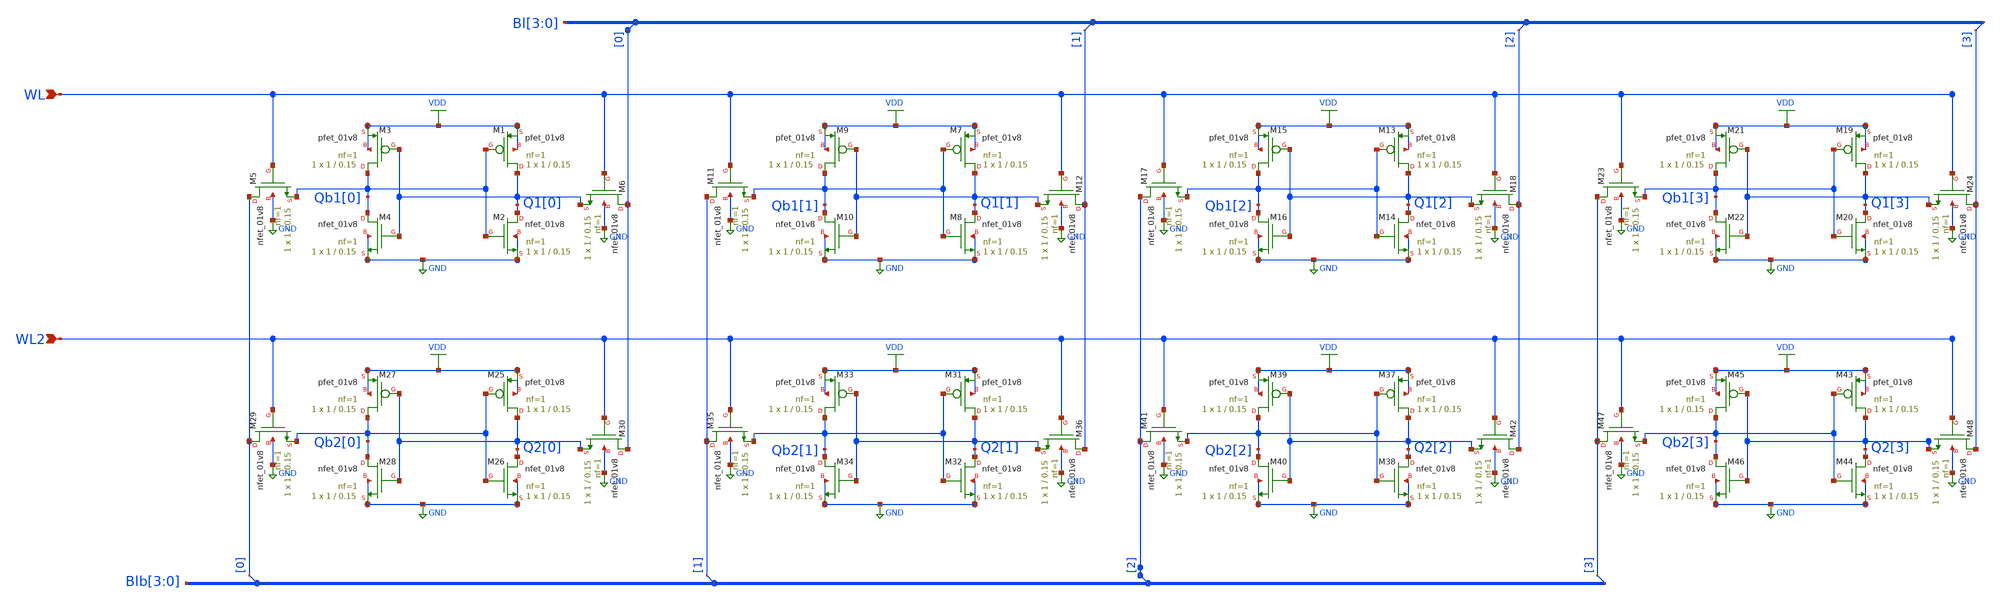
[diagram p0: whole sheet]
** sch_path: Circuit Files/circuits/circuits/RAM8BIT.sch
**.subckt RAM8BIT WL WL2
*.ipin WL
*.ipin WL2
XM1 Q1[0] Qb1[0] VDD VDD sky130_fd_pr__pfet_01v8 L=0.15 W=1 nf=1 ad='int((nf+1)/2) * W/nf * 0.29' as='int((nf+2)/2) * W/nf * 0.29'
+ pd='2*int((nf+1)/2) * (W/nf + 0.29)' ps='2*int((nf+2)/2) * (W/nf + 0.29)' nrd='0.29 / W' nrs='0.29 / W'
+ sa=0 sb=0 sd=0 mult=1 m=1
XM2 Q1[0] Qb1[0] GND GND sky130_fd_pr__nfet_01v8 L=0.15 W=1 nf=1 ad='int((nf+1)/2) * W/nf * 0.29' as='int((nf+2)/2) * W/nf * 0.29'
+ pd='2*int((nf+1)/2) * (W/nf + 0.29)' ps='2*int((nf+2)/2) * (W/nf + 0.29)' nrd='0.29 / W' nrs='0.29 / W'
+ sa=0 sb=0 sd=0 mult=1 m=1
XM3 Qb1[0] Q1[0] VDD VDD sky130_fd_pr__pfet_01v8 L=0.15 W=1 nf=1 ad='int((nf+1)/2) * W/nf * 0.29' as='int((nf+2)/2) * W/nf * 0.29'
+ pd='2*int((nf+1)/2) * (W/nf + 0.29)' ps='2*int((nf+2)/2) * (W/nf + 0.29)' nrd='0.29 / W' nrs='0.29 / W'
+ sa=0 sb=0 sd=0 mult=1 m=1
XM4 Qb1[0] Q1[0] GND GND sky130_fd_pr__nfet_01v8 L=0.15 W=1 nf=1 ad='int((nf+1)/2) * W/nf * 0.29' as='int((nf+2)/2) * W/nf * 0.29'
+ pd='2*int((nf+1)/2) * (W/nf + 0.29)' ps='2*int((nf+2)/2) * (W/nf + 0.29)' nrd='0.29 / W' nrs='0.29 / W'
+ sa=0 sb=0 sd=0 mult=1 m=1
XM5 Blb[0] WL Qb1[0] GND sky130_fd_pr__nfet_01v8 L=0.15 W=1 nf=1 ad='int((nf+1)/2) * W/nf * 0.29' as='int((nf+2)/2) * W/nf * 0.29'
+ pd='2*int((nf+1)/2) * (W/nf + 0.29)' ps='2*int((nf+2)/2) * (W/nf + 0.29)' nrd='0.29 / W' nrs='0.29 / W'
+ sa=0 sb=0 sd=0 mult=1 m=1
XM6 Bl[0] WL Q1[0] GND sky130_fd_pr__nfet_01v8 L=0.15 W=1 nf=1 ad='int((nf+1)/2) * W/nf * 0.29' as='int((nf+2)/2) * W/nf * 0.29'
+ pd='2*int((nf+1)/2) * (W/nf + 0.29)' ps='2*int((nf+2)/2) * (W/nf + 0.29)' nrd='0.29 / W' nrs='0.29 / W'
+ sa=0 sb=0 sd=0 mult=1 m=1
XM7 Q1[1] Qb1[1] VDD VDD sky130_fd_pr__pfet_01v8 L=0.15 W=1 nf=1 ad='int((nf+1)/2) * W/nf * 0.29' as='int((nf+2)/2) * W/nf * 0.29'
+ pd='2*int((nf+1)/2) * (W/nf + 0.29)' ps='2*int((nf+2)/2) * (W/nf + 0.29)' nrd='0.29 / W' nrs='0.29 / W'
+ sa=0 sb=0 sd=0 mult=1 m=1
XM8 Q1[1] Qb1[1] GND GND sky130_fd_pr__nfet_01v8 L=0.15 W=1 nf=1 ad='int((nf+1)/2) * W/nf * 0.29' as='int((nf+2)/2) * W/nf * 0.29'
+ pd='2*int((nf+1)/2) * (W/nf + 0.29)' ps='2*int((nf+2)/2) * (W/nf + 0.29)' nrd='0.29 / W' nrs='0.29 / W'
+ sa=0 sb=0 sd=0 mult=1 m=1
XM9 Qb1[1] Q1[1] VDD VDD sky130_fd_pr__pfet_01v8 L=0.15 W=1 nf=1 ad='int((nf+1)/2) * W/nf * 0.29' as='int((nf+2)/2) * W/nf * 0.29'
+ pd='2*int((nf+1)/2) * (W/nf + 0.29)' ps='2*int((nf+2)/2) * (W/nf + 0.29)' nrd='0.29 / W' nrs='0.29 / W'
+ sa=0 sb=0 sd=0 mult=1 m=1
XM10 Qb1[1] Q1[1] GND GND sky130_fd_pr__nfet_01v8 L=0.15 W=1 nf=1 ad='int((nf+1)/2) * W/nf * 0.29' as='int((nf+2)/2) * W/nf * 0.29'
+ pd='2*int((nf+1)/2) * (W/nf + 0.29)' ps='2*int((nf+2)/2) * (W/nf + 0.29)' nrd='0.29 / W' nrs='0.29 / W'
+ sa=0 sb=0 sd=0 mult=1 m=1
XM11 Blb[1] WL Qb1[1] GND sky130_fd_pr__nfet_01v8 L=0.15 W=1 nf=1 ad='int((nf+1)/2) * W/nf * 0.29' as='int((nf+2)/2) * W/nf * 0.29'
+ pd='2*int((nf+1)/2) * (W/nf + 0.29)' ps='2*int((nf+2)/2) * (W/nf + 0.29)' nrd='0.29 / W' nrs='0.29 / W'
+ sa=0 sb=0 sd=0 mult=1 m=1
XM12 Bl[1] WL Q1[1] GND sky130_fd_pr__nfet_01v8 L=0.15 W=1 nf=1 ad='int((nf+1)/2) * W/nf * 0.29' as='int((nf+2)/2) * W/nf * 0.29'
+ pd='2*int((nf+1)/2) * (W/nf + 0.29)' ps='2*int((nf+2)/2) * (W/nf + 0.29)' nrd='0.29 / W' nrs='0.29 / W'
+ sa=0 sb=0 sd=0 mult=1 m=1
XM13 Q1[2] Qb1[2] VDD VDD sky130_fd_pr__pfet_01v8 L=0.15 W=1 nf=1 ad='int((nf+1)/2) * W/nf * 0.29' as='int((nf+2)/2) * W/nf * 0.29'
+ pd='2*int((nf+1)/2) * (W/nf + 0.29)' ps='2*int((nf+2)/2) * (W/nf + 0.29)' nrd='0.29 / W' nrs='0.29 / W'
+ sa=0 sb=0 sd=0 mult=1 m=1
XM14 Q1[2] Qb1[2] GND GND sky130_fd_pr__nfet_01v8 L=0.15 W=1 nf=1 ad='int((nf+1)/2) * W/nf * 0.29' as='int((nf+2)/2) * W/nf * 0.29'
+ pd='2*int((nf+1)/2) * (W/nf + 0.29)' ps='2*int((nf+2)/2) * (W/nf + 0.29)' nrd='0.29 / W' nrs='0.29 / W'
+ sa=0 sb=0 sd=0 mult=1 m=1
XM15 Qb1[2] Q1[2] VDD VDD sky130_fd_pr__pfet_01v8 L=0.15 W=1 nf=1 ad='int((nf+1)/2) * W/nf * 0.29' as='int((nf+2)/2) * W/nf * 0.29'
+ pd='2*int((nf+1)/2) * (W/nf + 0.29)' ps='2*int((nf+2)/2) * (W/nf + 0.29)' nrd='0.29 / W' nrs='0.29 / W'
+ sa=0 sb=0 sd=0 mult=1 m=1
XM16 Qb1[2] Q1[2] GND GND sky130_fd_pr__nfet_01v8 L=0.15 W=1 nf=1 ad='int((nf+1)/2) * W/nf * 0.29' as='int((nf+2)/2) * W/nf * 0.29'
+ pd='2*int((nf+1)/2) * (W/nf + 0.29)' ps='2*int((nf+2)/2) * (W/nf + 0.29)' nrd='0.29 / W' nrs='0.29 / W'
+ sa=0 sb=0 sd=0 mult=1 m=1
XM17 Blb[2] WL Qb1[2] GND sky130_fd_pr__nfet_01v8 L=0.15 W=1 nf=1 ad='int((nf+1)/2) * W/nf * 0.29' as='int((nf+2)/2) * W/nf * 0.29'
+ pd='2*int((nf+1)/2) * (W/nf + 0.29)' ps='2*int((nf+2)/2) * (W/nf + 0.29)' nrd='0.29 / W' nrs='0.29 / W'
+ sa=0 sb=0 sd=0 mult=1 m=1
XM18 Bl[2] WL Q1[2] GND sky130_fd_pr__nfet_01v8 L=0.15 W=1 nf=1 ad='int((nf+1)/2) * W/nf * 0.29' as='int((nf+2)/2) * W/nf * 0.29'
+ pd='2*int((nf+1)/2) * (W/nf + 0.29)' ps='2*int((nf+2)/2) * (W/nf + 0.29)' nrd='0.29 / W' nrs='0.29 / W'
+ sa=0 sb=0 sd=0 mult=1 m=1
XM19 Q1[3] Qb1[3] VDD VDD sky130_fd_pr__pfet_01v8 L=0.15 W=1 nf=1 ad='int((nf+1)/2) * W/nf * 0.29' as='int((nf+2)/2) * W/nf * 0.29'
+ pd='2*int((nf+1)/2) * (W/nf + 0.29)' ps='2*int((nf+2)/2) * (W/nf + 0.29)' nrd='0.29 / W' nrs='0.29 / W'
+ sa=0 sb=0 sd=0 mult=1 m=1
XM20 Q1[3] Qb1[3] GND GND sky130_fd_pr__nfet_01v8 L=0.15 W=1 nf=1 ad='int((nf+1)/2) * W/nf * 0.29' as='int((nf+2)/2) * W/nf * 0.29'
+ pd='2*int((nf+1)/2) * (W/nf + 0.29)' ps='2*int((nf+2)/2) * (W/nf + 0.29)' nrd='0.29 / W' nrs='0.29 / W'
+ sa=0 sb=0 sd=0 mult=1 m=1
XM21 Qb1[3] Q1[3] VDD VDD sky130_fd_pr__pfet_01v8 L=0.15 W=1 nf=1 ad='int((nf+1)/2) * W/nf * 0.29' as='int((nf+2)/2) * W/nf * 0.29'
+ pd='2*int((nf+1)/2) * (W/nf + 0.29)' ps='2*int((nf+2)/2) * (W/nf + 0.29)' nrd='0.29 / W' nrs='0.29 / W'
+ sa=0 sb=0 sd=0 mult=1 m=1
XM22 Qb1[3] Q1[3] GND GND sky130_fd_pr__nfet_01v8 L=0.15 W=1 nf=1 ad='int((nf+1)/2) * W/nf * 0.29' as='int((nf+2)/2) * W/nf * 0.29'
+ pd='2*int((nf+1)/2) * (W/nf + 0.29)' ps='2*int((nf+2)/2) * (W/nf + 0.29)' nrd='0.29 / W' nrs='0.29 / W'
+ sa=0 sb=0 sd=0 mult=1 m=1
XM23 Blb[3] WL Qb1[3] GND sky130_fd_pr__nfet_01v8 L=0.15 W=1 nf=1 ad='int((nf+1)/2) * W/nf * 0.29' as='int((nf+2)/2) * W/nf * 0.29'
+ pd='2*int((nf+1)/2) * (W/nf + 0.29)' ps='2*int((nf+2)/2) * (W/nf + 0.29)' nrd='0.29 / W' nrs='0.29 / W'
+ sa=0 sb=0 sd=0 mult=1 m=1
XM24 Bl[3] WL Q1[3] GND sky130_fd_pr__nfet_01v8 L=0.15 W=1 nf=1 ad='int((nf+1)/2) * W/nf * 0.29' as='int((nf+2)/2) * W/nf * 0.29'
+ pd='2*int((nf+1)/2) * (W/nf + 0.29)' ps='2*int((nf+2)/2) * (W/nf + 0.29)' nrd='0.29 / W' nrs='0.29 / W'
+ sa=0 sb=0 sd=0 mult=1 m=1
XM25 Q2[0] Qb2[0] VDD VDD sky130_fd_pr__pfet_01v8 L=0.15 W=1 nf=1 ad='int((nf+1)/2) * W/nf * 0.29' as='int((nf+2)/2) * W/nf * 0.29'
+ pd='2*int((nf+1)/2) * (W/nf + 0.29)' ps='2*int((nf+2)/2) * (W/nf + 0.29)' nrd='0.29 / W' nrs='0.29 / W'
+ sa=0 sb=0 sd=0 mult=1 m=1
XM26 Q2[0] Qb2[0] GND GND sky130_fd_pr__nfet_01v8 L=0.15 W=1 nf=1 ad='int((nf+1)/2) * W/nf * 0.29' as='int((nf+2)/2) * W/nf * 0.29'
+ pd='2*int((nf+1)/2) * (W/nf + 0.29)' ps='2*int((nf+2)/2) * (W/nf + 0.29)' nrd='0.29 / W' nrs='0.29 / W'
+ sa=0 sb=0 sd=0 mult=1 m=1
XM27 Qb2[0] Q2[0] VDD VDD sky130_fd_pr__pfet_01v8 L=0.15 W=1 nf=1 ad='int((nf+1)/2) * W/nf * 0.29' as='int((nf+2)/2) * W/nf * 0.29'
+ pd='2*int((nf+1)/2) * (W/nf + 0.29)' ps='2*int((nf+2)/2) * (W/nf + 0.29)' nrd='0.29 / W' nrs='0.29 / W'
+ sa=0 sb=0 sd=0 mult=1 m=1
XM28 Qb2[0] Q2[0] GND GND sky130_fd_pr__nfet_01v8 L=0.15 W=1 nf=1 ad='int((nf+1)/2) * W/nf * 0.29' as='int((nf+2)/2) * W/nf * 0.29'
+ pd='2*int((nf+1)/2) * (W/nf + 0.29)' ps='2*int((nf+2)/2) * (W/nf + 0.29)' nrd='0.29 / W' nrs='0.29 / W'
+ sa=0 sb=0 sd=0 mult=1 m=1
XM29 Blb[0] WL2 Qb2[0] GND sky130_fd_pr__nfet_01v8 L=0.15 W=1 nf=1 ad='int((nf+1)/2) * W/nf * 0.29' as='int((nf+2)/2) * W/nf * 0.29'
+ pd='2*int((nf+1)/2) * (W/nf + 0.29)' ps='2*int((nf+2)/2) * (W/nf + 0.29)' nrd='0.29 / W' nrs='0.29 / W'
+ sa=0 sb=0 sd=0 mult=1 m=1
XM30 Bl[0] WL2 Q2[0] GND sky130_fd_pr__nfet_01v8 L=0.15 W=1 nf=1 ad='int((nf+1)/2) * W/nf * 0.29' as='int((nf+2)/2) * W/nf * 0.29'
+ pd='2*int((nf+1)/2) * (W/nf + 0.29)' ps='2*int((nf+2)/2) * (W/nf + 0.29)' nrd='0.29 / W' nrs='0.29 / W'
+ sa=0 sb=0 sd=0 mult=1 m=1
XM31 Q2[1] Qb2[1] VDD VDD sky130_fd_pr__pfet_01v8 L=0.15 W=1 nf=1 ad='int((nf+1)/2) * W/nf * 0.29' as='int((nf+2)/2) * W/nf * 0.29'
+ pd='2*int((nf+1)/2) * (W/nf + 0.29)' ps='2*int((nf+2)/2) * (W/nf + 0.29)' nrd='0.29 / W' nrs='0.29 / W'
+ sa=0 sb=0 sd=0 mult=1 m=1
XM32 Q2[1] Qb2[1] GND GND sky130_fd_pr__nfet_01v8 L=0.15 W=1 nf=1 ad='int((nf+1)/2) * W/nf * 0.29' as='int((nf+2)/2) * W/nf * 0.29'
+ pd='2*int((nf+1)/2) * (W/nf + 0.29)' ps='2*int((nf+2)/2) * (W/nf + 0.29)' nrd='0.29 / W' nrs='0.29 / W'
+ sa=0 sb=0 sd=0 mult=1 m=1
XM33 Qb2[1] Q2[1] VDD VDD sky130_fd_pr__pfet_01v8 L=0.15 W=1 nf=1 ad='int((nf+1)/2) * W/nf * 0.29' as='int((nf+2)/2) * W/nf * 0.29'
+ pd='2*int((nf+1)/2) * (W/nf + 0.29)' ps='2*int((nf+2)/2) * (W/nf + 0.29)' nrd='0.29 / W' nrs='0.29 / W'
+ sa=0 sb=0 sd=0 mult=1 m=1
XM34 Qb2[1] Q2[1] GND GND sky130_fd_pr__nfet_01v8 L=0.15 W=1 nf=1 ad='int((nf+1)/2) * W/nf * 0.29' as='int((nf+2)/2) * W/nf * 0.29'
+ pd='2*int((nf+1)/2) * (W/nf + 0.29)' ps='2*int((nf+2)/2) * (W/nf + 0.29)' nrd='0.29 / W' nrs='0.29 / W'
+ sa=0 sb=0 sd=0 mult=1 m=1
XM35 Blb[1] WL2 Qb2[1] GND sky130_fd_pr__nfet_01v8 L=0.15 W=1 nf=1 ad='int((nf+1)/2) * W/nf * 0.29' as='int((nf+2)/2) * W/nf * 0.29'
+ pd='2*int((nf+1)/2) * (W/nf + 0.29)' ps='2*int((nf+2)/2) * (W/nf + 0.29)' nrd='0.29 / W' nrs='0.29 / W'
+ sa=0 sb=0 sd=0 mult=1 m=1
XM36 Bl[1] WL2 Q2[1] GND sky130_fd_pr__nfet_01v8 L=0.15 W=1 nf=1 ad='int((nf+1)/2) * W/nf * 0.29' as='int((nf+2)/2) * W/nf * 0.29'
+ pd='2*int((nf+1)/2) * (W/nf + 0.29)' ps='2*int((nf+2)/2) * (W/nf + 0.29)' nrd='0.29 / W' nrs='0.29 / W'
+ sa=0 sb=0 sd=0 mult=1 m=1
XM37 Q2[2] Qb2[2] VDD VDD sky130_fd_pr__pfet_01v8 L=0.15 W=1 nf=1 ad='int((nf+1)/2) * W/nf * 0.29' as='int((nf+2)/2) * W/nf * 0.29'
+ pd='2*int((nf+1)/2) * (W/nf + 0.29)' ps='2*int((nf+2)/2) * (W/nf + 0.29)' nrd='0.29 / W' nrs='0.29 / W'
+ sa=0 sb=0 sd=0 mult=1 m=1
XM38 Q2[2] Qb2[2] GND GND sky130_fd_pr__nfet_01v8 L=0.15 W=1 nf=1 ad='int((nf+1)/2) * W/nf * 0.29' as='int((nf+2)/2) * W/nf * 0.29'
+ pd='2*int((nf+1)/2) * (W/nf + 0.29)' ps='2*int((nf+2)/2) * (W/nf + 0.29)' nrd='0.29 / W' nrs='0.29 / W'
+ sa=0 sb=0 sd=0 mult=1 m=1
XM39 Qb2[2] Q2[2] VDD VDD sky130_fd_pr__pfet_01v8 L=0.15 W=1 nf=1 ad='int((nf+1)/2) * W/nf * 0.29' as='int((nf+2)/2) * W/nf * 0.29'
+ pd='2*int((nf+1)/2) * (W/nf + 0.29)' ps='2*int((nf+2)/2) * (W/nf + 0.29)' nrd='0.29 / W' nrs='0.29 / W'
+ sa=0 sb=0 sd=0 mult=1 m=1
XM40 Qb2[2] Q2[2] GND GND sky130_fd_pr__nfet_01v8 L=0.15 W=1 nf=1 ad='int((nf+1)/2) * W/nf * 0.29' as='int((nf+2)/2) * W/nf * 0.29'
+ pd='2*int((nf+1)/2) * (W/nf + 0.29)' ps='2*int((nf+2)/2) * (W/nf + 0.29)' nrd='0.29 / W' nrs='0.29 / W'
+ sa=0 sb=0 sd=0 mult=1 m=1
XM41 Blb[2] WL2 Qb2[2] GND sky130_fd_pr__nfet_01v8 L=0.15 W=1 nf=1 ad='int((nf+1)/2) * W/nf * 0.29' as='int((nf+2)/2) * W/nf * 0.29'
+ pd='2*int((nf+1)/2) * (W/nf + 0.29)' ps='2*int((nf+2)/2) * (W/nf + 0.29)' nrd='0.29 / W' nrs='0.29 / W'
+ sa=0 sb=0 sd=0 mult=1 m=1
XM42 Bl[2] WL2 Q2[2] GND sky130_fd_pr__nfet_01v8 L=0.15 W=1 nf=1 ad='int((nf+1)/2) * W/nf * 0.29' as='int((nf+2)/2) * W/nf * 0.29'
+ pd='2*int((nf+1)/2) * (W/nf + 0.29)' ps='2*int((nf+2)/2) * (W/nf + 0.29)' nrd='0.29 / W' nrs='0.29 / W'
+ sa=0 sb=0 sd=0 mult=1 m=1
XM43 Q2[3] Qb2[3] VDD VDD sky130_fd_pr__pfet_01v8 L=0.15 W=1 nf=1 ad='int((nf+1)/2) * W/nf * 0.29' as='int((nf+2)/2) * W/nf * 0.29'
+ pd='2*int((nf+1)/2) * (W/nf + 0.29)' ps='2*int((nf+2)/2) * (W/nf + 0.29)' nrd='0.29 / W' nrs='0.29 / W'
+ sa=0 sb=0 sd=0 mult=1 m=1
XM44 Q2[3] Qb2[3] GND GND sky130_fd_pr__nfet_01v8 L=0.15 W=1 nf=1 ad='int((nf+1)/2) * W/nf * 0.29' as='int((nf+2)/2) * W/nf * 0.29'
+ pd='2*int((nf+1)/2) * (W/nf + 0.29)' ps='2*int((nf+2)/2) * (W/nf + 0.29)' nrd='0.29 / W' nrs='0.29 / W'
+ sa=0 sb=0 sd=0 mult=1 m=1
XM45 Qb2[3] Q2[3] VDD VDD sky130_fd_pr__pfet_01v8 L=0.15 W=1 nf=1 ad='int((nf+1)/2) * W/nf * 0.29' as='int((nf+2)/2) * W/nf * 0.29'
+ pd='2*int((nf+1)/2) * (W/nf + 0.29)' ps='2*int((nf+2)/2) * (W/nf + 0.29)' nrd='0.29 / W' nrs='0.29 / W'
+ sa=0 sb=0 sd=0 mult=1 m=1
XM46 Qb2[3] Q2[3] GND GND sky130_fd_pr__nfet_01v8 L=0.15 W=1 nf=1 ad='int((nf+1)/2) * W/nf * 0.29' as='int((nf+2)/2) * W/nf * 0.29'
+ pd='2*int((nf+1)/2) * (W/nf + 0.29)' ps='2*int((nf+2)/2) * (W/nf + 0.29)' nrd='0.29 / W' nrs='0.29 / W'
+ sa=0 sb=0 sd=0 mult=1 m=1
XM47 Blb[3] WL2 Qb2[3] GND sky130_fd_pr__nfet_01v8 L=0.15 W=1 nf=1 ad='int((nf+1)/2) * W/nf * 0.29' as='int((nf+2)/2) * W/nf * 0.29'
+ pd='2*int((nf+1)/2) * (W/nf + 0.29)' ps='2*int((nf+2)/2) * (W/nf + 0.29)' nrd='0.29 / W' nrs='0.29 / W'
+ sa=0 sb=0 sd=0 mult=1 m=1
XM48 Bl[3] WL2 Q2[3] GND sky130_fd_pr__nfet_01v8 L=0.15 W=1 nf=1 ad='int((nf+1)/2) * W/nf * 0.29' as='int((nf+2)/2) * W/nf * 0.29'
+ pd='2*int((nf+1)/2) * (W/nf + 0.29)' ps='2*int((nf+2)/2) * (W/nf + 0.29)' nrd='0.29 / W' nrs='0.29 / W'
+ sa=0 sb=0 sd=0 mult=1 m=1
* tap: Bl[3:0] --> Bl[0]
* tap: Bl[3:0] --> Bl[1]
* tap: Bl[3:0] --> Bl[2]
* tap: Bl[3:0] --> Bl[3]
* tap: Blb[3:0] --> Blb[0]
* tap: Blb[3:0] --> Blb[1]
* tap: Blb[3:0] --> Blb[2]
* tap: Blb[3:0] --> Blb[3]
**** begin user architecture code

.lib /usr/local/share/pdk/sky130A/libs.tech/combined/sky130.lib.spice tt
vdd vdd 0 dc 2
Vwl1 wl 0 dc 0
Vwl2 wl2 0 dc pwl (0n 0 10n 0 10.1n 2 20n 2 20.1n 0 25.1n 0 25.2n 2 40n 2 40.1n 0)
vblb1 BLb[1] 0 dc 0
vbl1 Bl[1] 0 dc 0
vblb0 BLb[0] 0 dc 0
vbl0 Bl[0] 0 dc 0
vblb2 BLb[2] 0 dc 0
vbl2 Bl[2] 0 dc 0
vblb3 BLb[3] 0 dc pwl (0n 0 25.1n 0 25.2n 2 )
vbl3 Bl[3] 0 dc pwl (0n 0 10n 0 10.1n 2 20n 2 20.1n 0 25.1n 0 25.2n 2 )


.tran 0.1 400n
.save all


**** end user architecture code
**.ends
.GLOBAL GND
.GLOBAL VDD
.end
